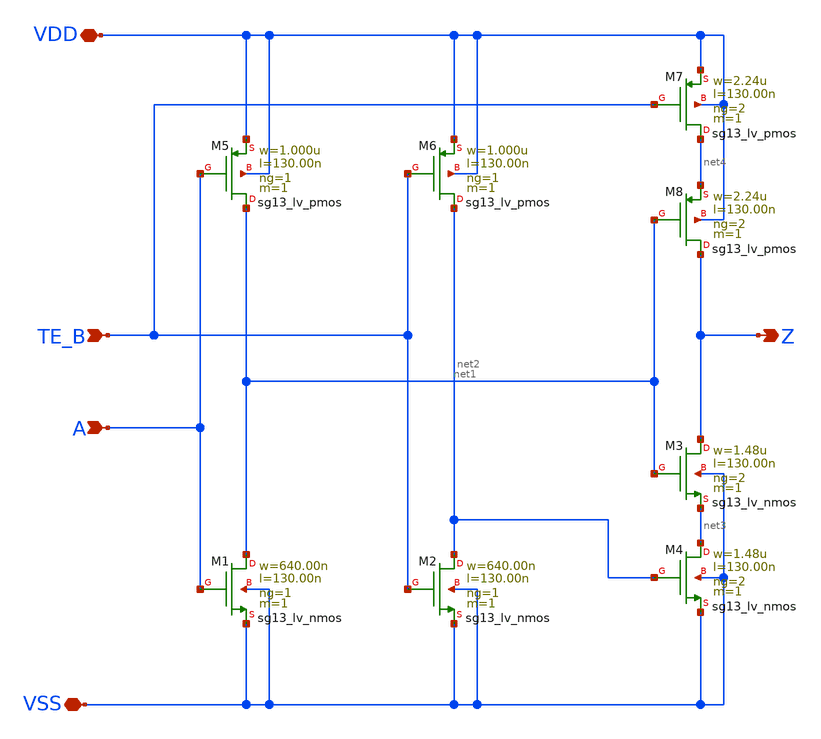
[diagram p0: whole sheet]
** sch_path: ihp-sg13g2/libs.tech/xschem/sg13g2_stdcells/sg13g2_ebufn_2.sch
* Copyright 2023 IHP PDK Authors
* Licensed under the Apache License, Version 2.0 (the "License");
* you may not use this file except in compliance with the License.
* You may obtain a copy of the License at
* https://www.apache.org/licenses/LICENSE-2.0
* Unless required by applicable law or agreed to in writing, software
* distributed under the License is distributed on an "AS IS" BASIS,
* WITHOUT WARRANTIES OR CONDITIONS OF ANY KIND, either express or implied.
* See the License for the specific language governing permissions and
* limitations under the License.
**.subckt sg13g2_ebufn_2 A TE_B Z VDD VSS
*.ipin A
*.ipin TE_B
*.opin Z
*.iopin VDD
*.iopin VSS
XM1 net1 A VSS VSS sg13_lv_nmos w=640.00n l=130.00n ng=1 m=1 mm_ok=1
XM2 net2 TE_B VSS VSS sg13_lv_nmos w=640.00n l=130.00n ng=1 m=1 mm_ok=1
XM3 Z net1 net3 VSS sg13_lv_nmos w=1.48u l=130.00n ng=2 m=1 mm_ok=1
XM4 net3 net2 VSS VSS sg13_lv_nmos w=1.48u l=130.00n ng=2 m=1 mm_ok=1
XM5 net1 A VDD VDD sg13_lv_pmos w=1.000u l=130.00n ng=1 m=1 mm_ok=1
XM6 net2 TE_B VDD VDD sg13_lv_pmos w=1.000u l=130.00n ng=1 m=1 mm_ok=1
XM7 net4 TE_B VDD VDD sg13_lv_pmos w=2.24u l=130.00n ng=2 m=1 mm_ok=1
XM8 Z net1 net4 VDD sg13_lv_pmos w=2.24u l=130.00n ng=2 m=1 mm_ok=1
**.ends
.end
